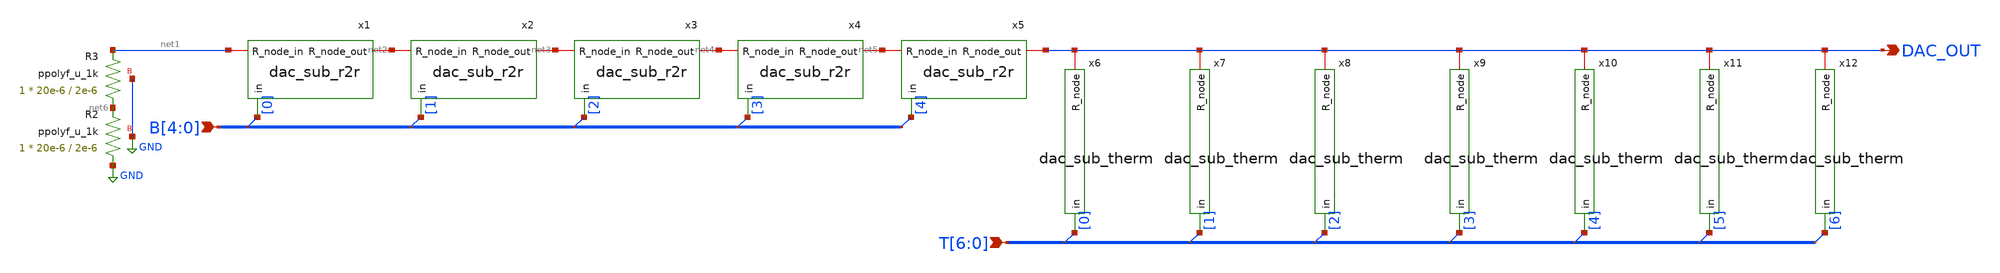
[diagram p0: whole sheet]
** sch_path: xschem/dac_seg_5_3.sch
**.subckt dac_seg_5_3 B[4],B[3],B[2],B[1],B[0] T[6],T[5],T[4],T[3],T[2],T[1],T[0] DAC_OUT
*.ipin B[4],B[3],B[2],B[1],B[0]
*.ipin T[6],T[5],T[4],T[3],T[2],T[1],T[0]
*.opin DAC_OUT
x1 net2 net1 B[0] dac_sub_r2r
x2 net3 net2 B[1] dac_sub_r2r
x3 net4 net3 B[2] dac_sub_r2r
x4 net5 net4 B[3] dac_sub_r2r
x5 DAC_OUT net5 B[4] dac_sub_r2r
* tap: B[4:0] --> B[0]
* tap: B[4:0] --> B[1]
* tap: B[4:0] --> B[2]
* tap: B[4:0] --> B[3]
* tap: B[4:0] --> B[4]
x6 DAC_OUT T[0] dac_sub_therm
x7 DAC_OUT T[1] dac_sub_therm
x8 DAC_OUT T[2] dac_sub_therm
x9 DAC_OUT T[3] dac_sub_therm
x10 DAC_OUT T[4] dac_sub_therm
x11 DAC_OUT T[5] dac_sub_therm
x12 DAC_OUT T[6] dac_sub_therm
* tap: T[6:0] --> T[0]
* tap: T[6:0] --> T[1]
* tap: T[6:0] --> T[2]
* tap: T[6:0] --> T[3]
* tap: T[6:0] --> T[4]
* tap: T[6:0] --> T[5]
* tap: T[6:0] --> T[6]
XR2 GND net6 GND ppolyf_u_1k r_width=20e-6 r_length=2e-6 m=1
XR3 net6 net1 GND ppolyf_u_1k r_width=20e-6 r_length=2e-6 m=1
**.ends

* expanding   symbol:  dac_sub_r2r.sym # of pins=3
** sym_path: xschem/dac_sub_r2r.sym
** sch_path: xschem/dac_sub_r2r.sch
.subckt dac_sub_r2r R_node_out R_node_in in
*.ipin in
*.iopin R_node_out
*.iopin R_node_in
XR7 in net1 GND ppolyf_u_1k r_width=20e-6 r_length=2e-6 m=1
XR1 net1 R_node_in GND ppolyf_u_1k r_width=20e-6 r_length=2e-6 m=1
XR2 net2 R_node_in GND ppolyf_u_1k r_width=20e-6 r_length=2e-6 m=1
XR3 R_node_out net2 GND ppolyf_u_1k r_width=20e-6 r_length=2e-6 m=1
XR4 net3 R_node_in GND ppolyf_u_1k r_width=20e-6 r_length=2e-6 m=1
XR5 R_node_out net3 GND ppolyf_u_1k r_width=20e-6 r_length=2e-6 m=1
.ends


* expanding   symbol:  dac_sub_therm.sym # of pins=2
** sym_path: xschem/dac_sub_therm.sym
** sch_path: xschem/dac_sub_therm.sch
.subckt dac_sub_therm R_node in
*.ipin in
*.iopin R_node
XR7 in net1 GND ppolyf_u_1k r_width=20e-6 r_length=2e-6 m=1
XR1 net1 R_node GND ppolyf_u_1k r_width=20e-6 r_length=2e-6 m=1
.ends

.GLOBAL GND
.end
